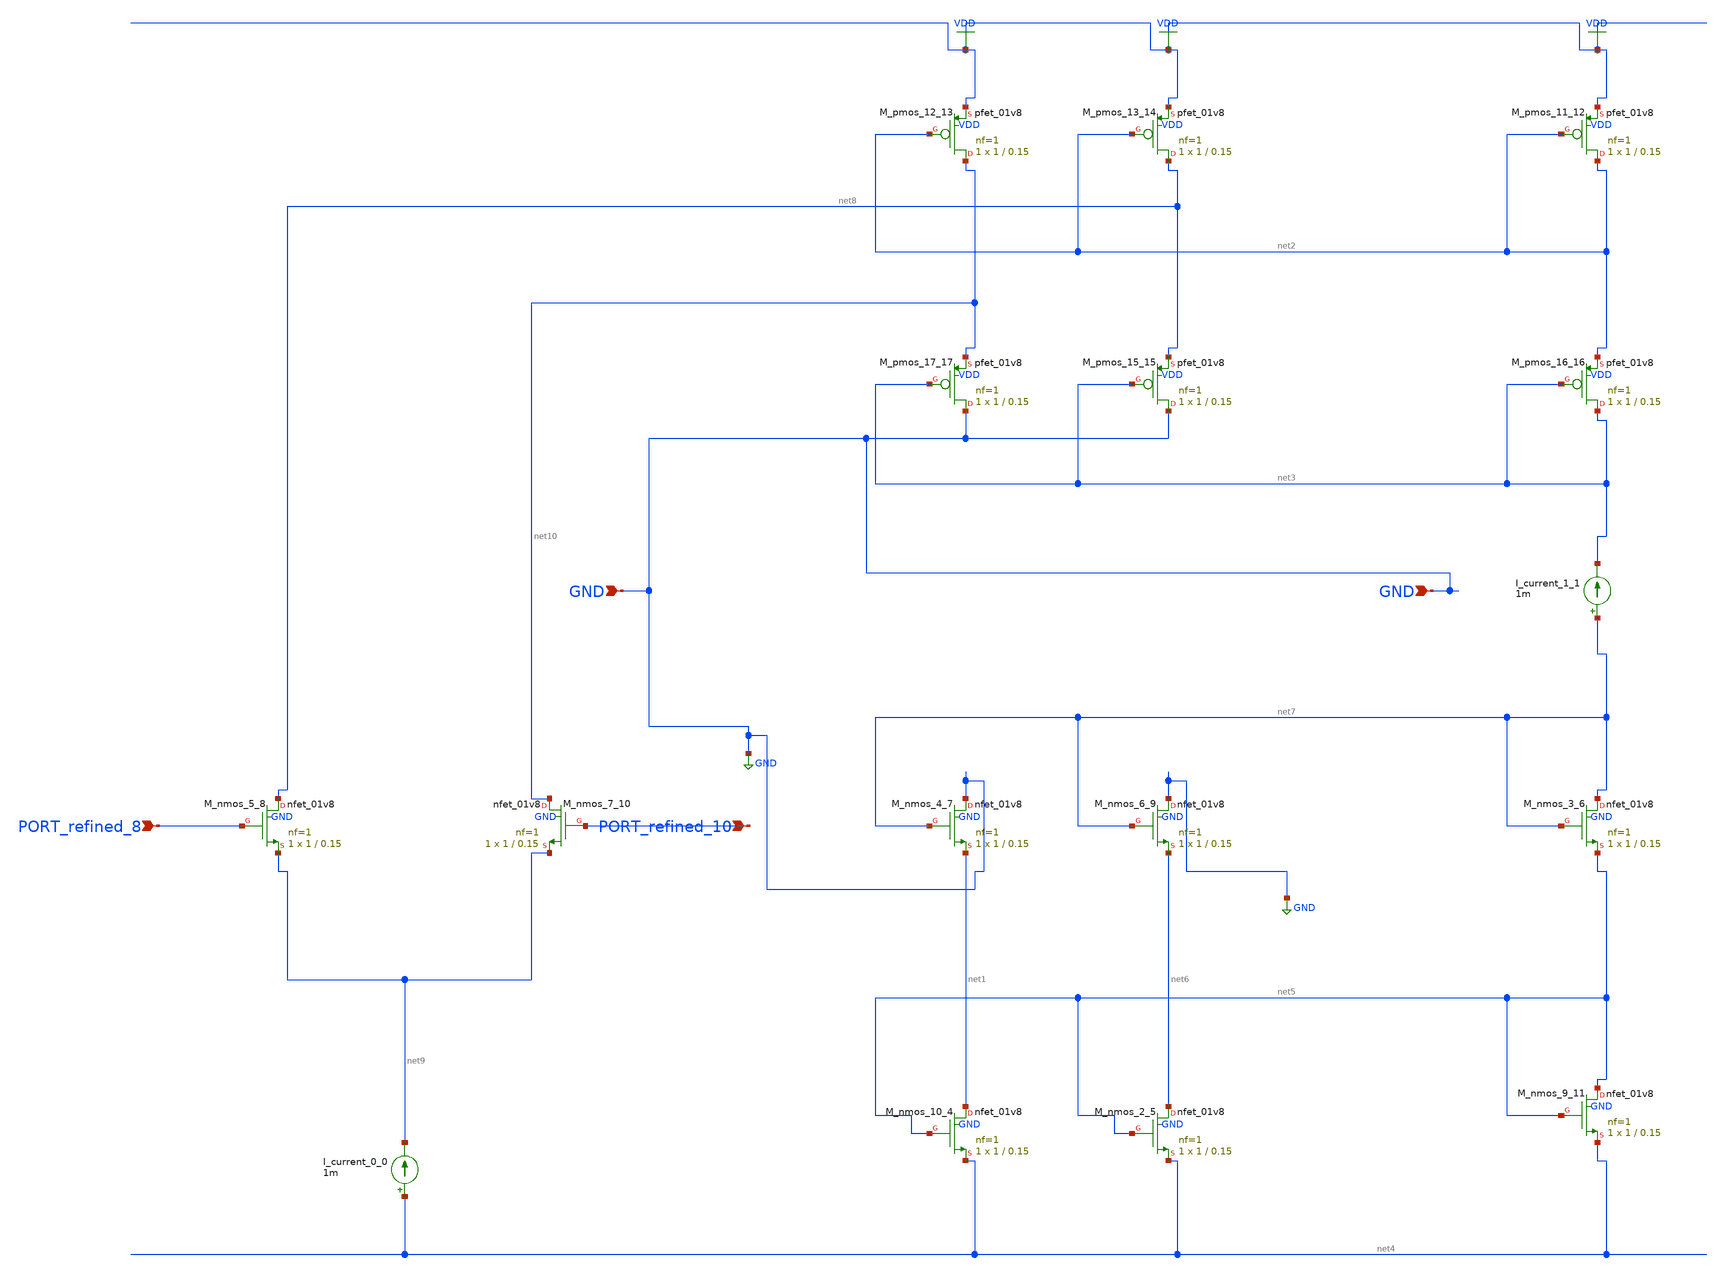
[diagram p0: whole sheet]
** sch_path: schematics/10_17485_IJST_v18i36_1552_05_001_canvas.sch
**.subckt 10_17485_IJST_v18i36_1552_05_001_canvas GND GND PORT_refined_10 PORT_refined_8
*.ipin GND
*.ipin GND
*.ipin PORT_refined_10
*.ipin PORT_refined_8
I_current_0_0 net4 net9 1m
I_current_1_1 net7 net3 1m
XM_nmos_10_4 net1 net5 net4 GND sky130_fd_pr__nfet_01v8 L=0.15 W=1 nf=1 ad='int((1 + 1)/2) * 1 / 1 * 0.29'
+ as='int((1 + 2)/2) * 1 / 1 * 0.29' pd='2*int((1 + 1)/2) * (1 / 1 + 0.29)' ps='2*int((1 + 2)/2) * (1 / 1 + 0.29)'
+ nrd='0.29 / 1 ' nrs='0.29 / 1 ' sa=0 sb=0 sd=0 mult=1 m=1
XM_nmos_2_5 net6 net5 net4 GND sky130_fd_pr__nfet_01v8 L=0.15 W=1 nf=1 ad='int((1 + 1)/2) * 1 / 1 * 0.29'
+ as='int((1 + 2)/2) * 1 / 1 * 0.29' pd='2*int((1 + 1)/2) * (1 / 1 + 0.29)' ps='2*int((1 + 2)/2) * (1 / 1 + 0.29)'
+ nrd='0.29 / 1 ' nrs='0.29 / 1 ' sa=0 sb=0 sd=0 mult=1 m=1
XM_nmos_3_6 net7 net7 net5 GND sky130_fd_pr__nfet_01v8 L=0.15 W=1 nf=1 ad='int((1 + 1)/2) * 1 / 1 * 0.29'
+ as='int((1 + 2)/2) * 1 / 1 * 0.29' pd='2*int((1 + 1)/2) * (1 / 1 + 0.29)' ps='2*int((1 + 2)/2) * (1 / 1 + 0.29)'
+ nrd='0.29 / 1 ' nrs='0.29 / 1 ' sa=0 sb=0 sd=0 mult=1 m=1
XM_nmos_4_7 GND net7 net1 GND sky130_fd_pr__nfet_01v8 L=0.15 W=1 nf=1 ad='int((1 + 1)/2) * 1 / 1 * 0.29'
+ as='int((1 + 2)/2) * 1 / 1 * 0.29' pd='2*int((1 + 1)/2) * (1 / 1 + 0.29)' ps='2*int((1 + 2)/2) * (1 / 1 + 0.29)'
+ nrd='0.29 / 1 ' nrs='0.29 / 1 ' sa=0 sb=0 sd=0 mult=1 m=1
XM_nmos_5_8 net8 PORT_refined_8 net9 GND sky130_fd_pr__nfet_01v8 L=0.15 W=1 nf=1 ad='int((1 + 1)/2) * 1 / 1 * 0.29'
+ as='int((1 + 2)/2) * 1 / 1 * 0.29' pd='2*int((1 + 1)/2) * (1 / 1 + 0.29)' ps='2*int((1 + 2)/2) * (1 / 1 + 0.29)'
+ nrd='0.29 / 1 ' nrs='0.29 / 1 ' sa=0 sb=0 sd=0 mult=1 m=1
XM_nmos_6_9 GND net7 net6 GND sky130_fd_pr__nfet_01v8 L=0.15 W=1 nf=1 ad='int((1 + 1)/2) * 1 / 1 * 0.29'
+ as='int((1 + 2)/2) * 1 / 1 * 0.29' pd='2*int((1 + 1)/2) * (1 / 1 + 0.29)' ps='2*int((1 + 2)/2) * (1 / 1 + 0.29)'
+ nrd='0.29 / 1 ' nrs='0.29 / 1 ' sa=0 sb=0 sd=0 mult=1 m=1
XM_nmos_7_10 net10 PORT_refined_10 net9 GND sky130_fd_pr__nfet_01v8 L=0.15 W=1 nf=1 ad='int((1 + 1)/2) * 1 / 1 * 0.29'
+ as='int((1 + 2)/2) * 1 / 1 * 0.29' pd='2*int((1 + 1)/2) * (1 / 1 + 0.29)' ps='2*int((1 + 2)/2) * (1 / 1 + 0.29)'
+ nrd='0.29 / 1 ' nrs='0.29 / 1 ' sa=0 sb=0 sd=0 mult=1 m=1
XM_nmos_9_11 net5 net5 net4 GND sky130_fd_pr__nfet_01v8 L=0.15 W=1 nf=1 ad='int((1 + 1)/2) * 1 / 1 * 0.29'
+ as='int((1 + 2)/2) * 1 / 1 * 0.29' pd='2*int((1 + 1)/2) * (1 / 1 + 0.29)' ps='2*int((1 + 2)/2) * (1 / 1 + 0.29)'
+ nrd='0.29 / 1 ' nrs='0.29 / 1 ' sa=0 sb=0 sd=0 mult=1 m=1
XM_pmos_11_12 net2 net2 VDD VDD sky130_fd_pr__pfet_01v8 L=0.15 W=1 nf=1 ad='int((1 + 1)/2) * 1 / 1 * 0.29'
+ as='int((1 + 2)/2) * 1 / 1 * 0.29' pd='2*int((1 + 1)/2) * (1 / 1 + 0.29)' ps='2*int((1 + 2)/2) * (1 / 1 + 0.29)'
+ nrd='0.29 / 1 ' nrs='0.29 / 1 ' sa=0 sb=0 sd=0 mult=1 m=1
XM_pmos_12_13 net10 net2 VDD VDD sky130_fd_pr__pfet_01v8 L=0.15 W=1 nf=1 ad='int((1 + 1)/2) * 1 / 1 * 0.29'
+ as='int((1 + 2)/2) * 1 / 1 * 0.29' pd='2*int((1 + 1)/2) * (1 / 1 + 0.29)' ps='2*int((1 + 2)/2) * (1 / 1 + 0.29)'
+ nrd='0.29 / 1 ' nrs='0.29 / 1 ' sa=0 sb=0 sd=0 mult=1 m=1
XM_pmos_13_14 net8 net2 VDD VDD sky130_fd_pr__pfet_01v8 L=0.15 W=1 nf=1 ad='int((1 + 1)/2) * 1 / 1 * 0.29'
+ as='int((1 + 2)/2) * 1 / 1 * 0.29' pd='2*int((1 + 1)/2) * (1 / 1 + 0.29)' ps='2*int((1 + 2)/2) * (1 / 1 + 0.29)'
+ nrd='0.29 / 1 ' nrs='0.29 / 1 ' sa=0 sb=0 sd=0 mult=1 m=1
XM_pmos_15_15 GND net3 net8 VDD sky130_fd_pr__pfet_01v8 L=0.15 W=1 nf=1 ad='int((1 + 1)/2) * 1 / 1 * 0.29'
+ as='int((1 + 2)/2) * 1 / 1 * 0.29' pd='2*int((1 + 1)/2) * (1 / 1 + 0.29)' ps='2*int((1 + 2)/2) * (1 / 1 + 0.29)'
+ nrd='0.29 / 1 ' nrs='0.29 / 1 ' sa=0 sb=0 sd=0 mult=1 m=1
XM_pmos_16_16 net3 net3 net2 VDD sky130_fd_pr__pfet_01v8 L=0.15 W=1 nf=1 ad='int((1 + 1)/2) * 1 / 1 * 0.29'
+ as='int((1 + 2)/2) * 1 / 1 * 0.29' pd='2*int((1 + 1)/2) * (1 / 1 + 0.29)' ps='2*int((1 + 2)/2) * (1 / 1 + 0.29)'
+ nrd='0.29 / 1 ' nrs='0.29 / 1 ' sa=0 sb=0 sd=0 mult=1 m=1
XM_pmos_17_17 GND net3 net10 VDD sky130_fd_pr__pfet_01v8 L=0.15 W=1 nf=1 ad='int((1 + 1)/2) * 1 / 1 * 0.29'
+ as='int((1 + 2)/2) * 1 / 1 * 0.29' pd='2*int((1 + 1)/2) * (1 / 1 + 0.29)' ps='2*int((1 + 2)/2) * (1 / 1 + 0.29)'
+ nrd='0.29 / 1 ' nrs='0.29 / 1 ' sa=0 sb=0 sd=0 mult=1 m=1
**.ends
.GLOBAL GND
.GLOBAL VDD
.end
